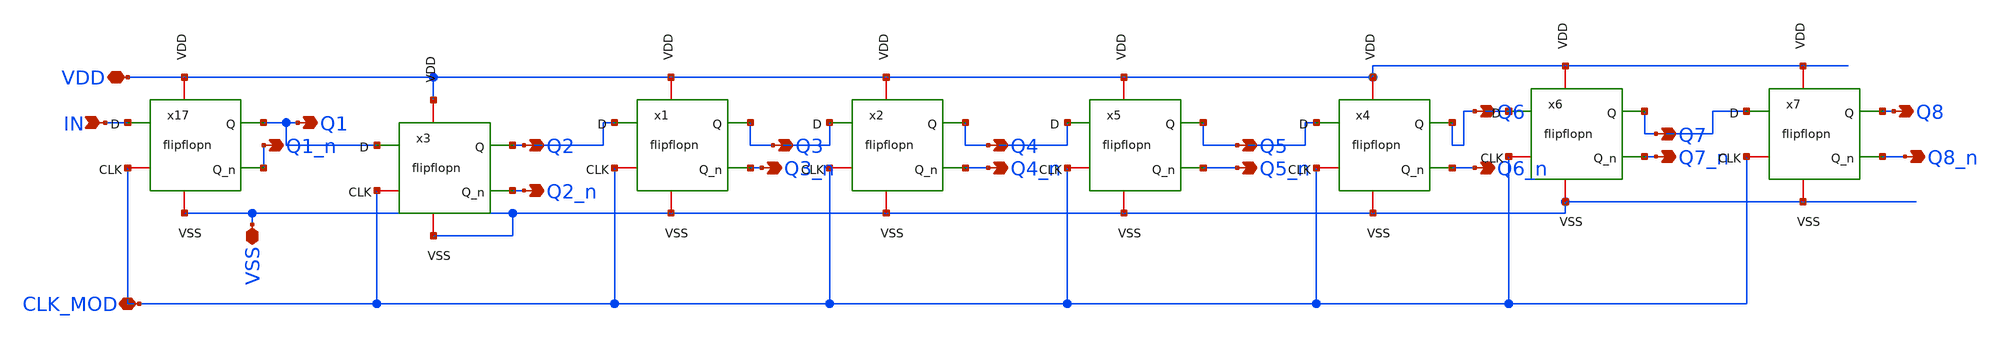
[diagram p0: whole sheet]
** sch_path: XSCHEM/shiftregn.sch
**.subckt shiftregn IN Q1 CLK_MOD VDD VSS Q2 Q3 Q4 Q5 Q6 Q7 Q8 Q1_n Q2_n Q3_n Q4_n Q5_n Q6_n Q7_n
*+ Q8_n
*.ipin IN
*.opin Q1
*.iopin CLK_MOD
*.iopin VDD
*.iopin VSS
*.opin Q2
*.opin Q3
*.opin Q4
*.opin Q5
*.opin Q6
*.opin Q7
*.opin Q8
*.opin Q1_n
*.opin Q2_n
*.opin Q3_n
*.opin Q4_n
*.opin Q5_n
*.opin Q6_n
*.opin Q7_n
*.opin Q8_n
x17 CLK_MOD Q1_n VDD Q1 IN VSS flipflopn
x1 CLK_MOD Q3_n VDD Q3 Q2 VSS flipflopn
x3 CLK_MOD Q2_n VDD Q2 Q1 VSS flipflopn
x2 CLK_MOD Q4_n VDD Q4 Q3 VSS flipflopn
x4 CLK_MOD Q6_n VDD Q6 Q5 VSS flipflopn
x5 CLK_MOD Q5_n VDD Q5 Q4 VSS flipflopn
x6 CLK_MOD Q7_n VDD Q7 Q6 VSS flipflopn
x7 CLK_MOD Q8_n VDD Q8 Q7 VSS flipflopn
**.ends

* expanding   symbol:  flipflopn.sym # of pins=6
** sym_path: flipflopn.sym
** sch_path: flipflopn.sch
.subckt flipflopn CLK Q_n VDD Q D VSS
*.ipin D
*.opin Q
*.iopin CLK
*.iopin VDD
*.iopin VSS
*.opin Q_n
XMN0 net1 net7 net2 VSS sg13_lv_nmos w=740.00n l=130.00n ng=1 m=1 mm_ok=1
XMP0 net1 CLK net2 VDD sg13_lv_pmos w=1.12u l=130.00n ng=1 m=1 mm_ok=1
XMN1 net2 CLK net3 VSS sg13_lv_nmos w=740.00n l=130.00n ng=1 m=1 mm_ok=1
XMP1 net2 net7 net3 VDD sg13_lv_pmos w=1.12u l=130.00n ng=1 m=1 mm_ok=1
XMN2 net4 CLK net5 VSS sg13_lv_nmos w=740.00n l=130.00n ng=1 m=1 mm_ok=1
XMP2 net4 net7 net5 VDD sg13_lv_pmos w=1.12u l=130.00n ng=1 m=1 mm_ok=1
XMN3 net5 net7 net6 VSS sg13_lv_nmos w=740.00n l=130.00n ng=1 m=1 mm_ok=1
XMP3 net5 CLK net6 VDD sg13_lv_pmos w=1.12u l=130.00n ng=1 m=1 mm_ok=1
x8 VDD net1 D VSS my_inv
x1 VDD net4 net2 VSS my_inv
x2 VDD net7 CLK VSS my_inv
x3 VDD net3 net4 VSS my_inv
x4 VDD Q_n net5 VSS my_inv
x5 VDD Q Q_n VSS my_inv
x6 VDD net6 Q_n VSS my_inv
.ends


* expanding   symbol:  my_inv.sym # of pins=4
** sym_path: xschem/my_inv.sym
** sch_path: xschem/my_inv.sch
.subckt my_inv VDD Y A VSS
*.opin Y
*.ipin A
*.iopin VDD
*.iopin VSS
XMN0 Y A VSS VSS sg13_lv_nmos w=740.00n l=130.00n ng=1 m=1 mm_ok=1
XMP0 Y A VDD VDD sg13_lv_pmos w=1.12u l=130.00n ng=1 m=1 mm_ok=1
.ends

.end
